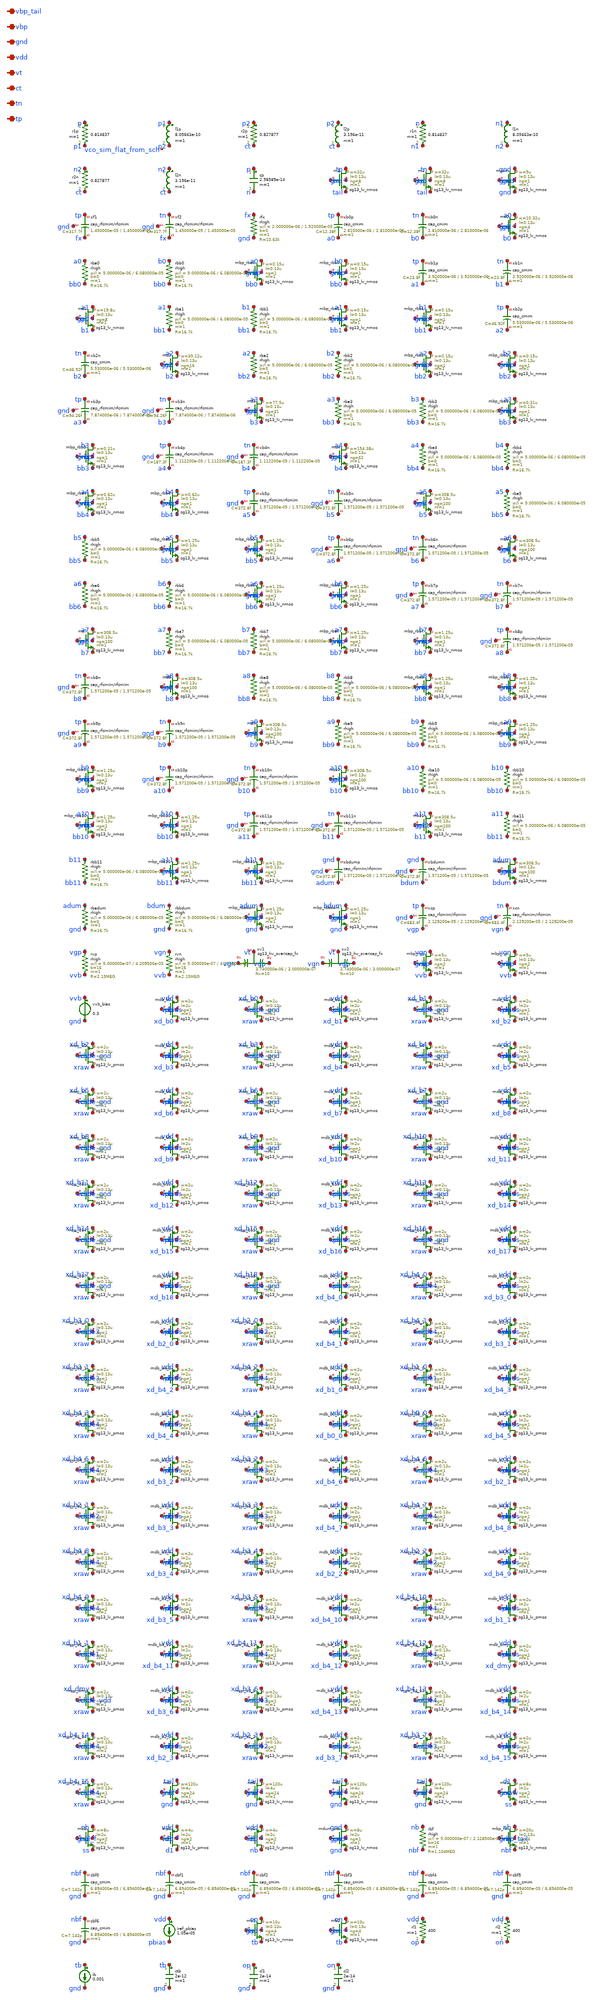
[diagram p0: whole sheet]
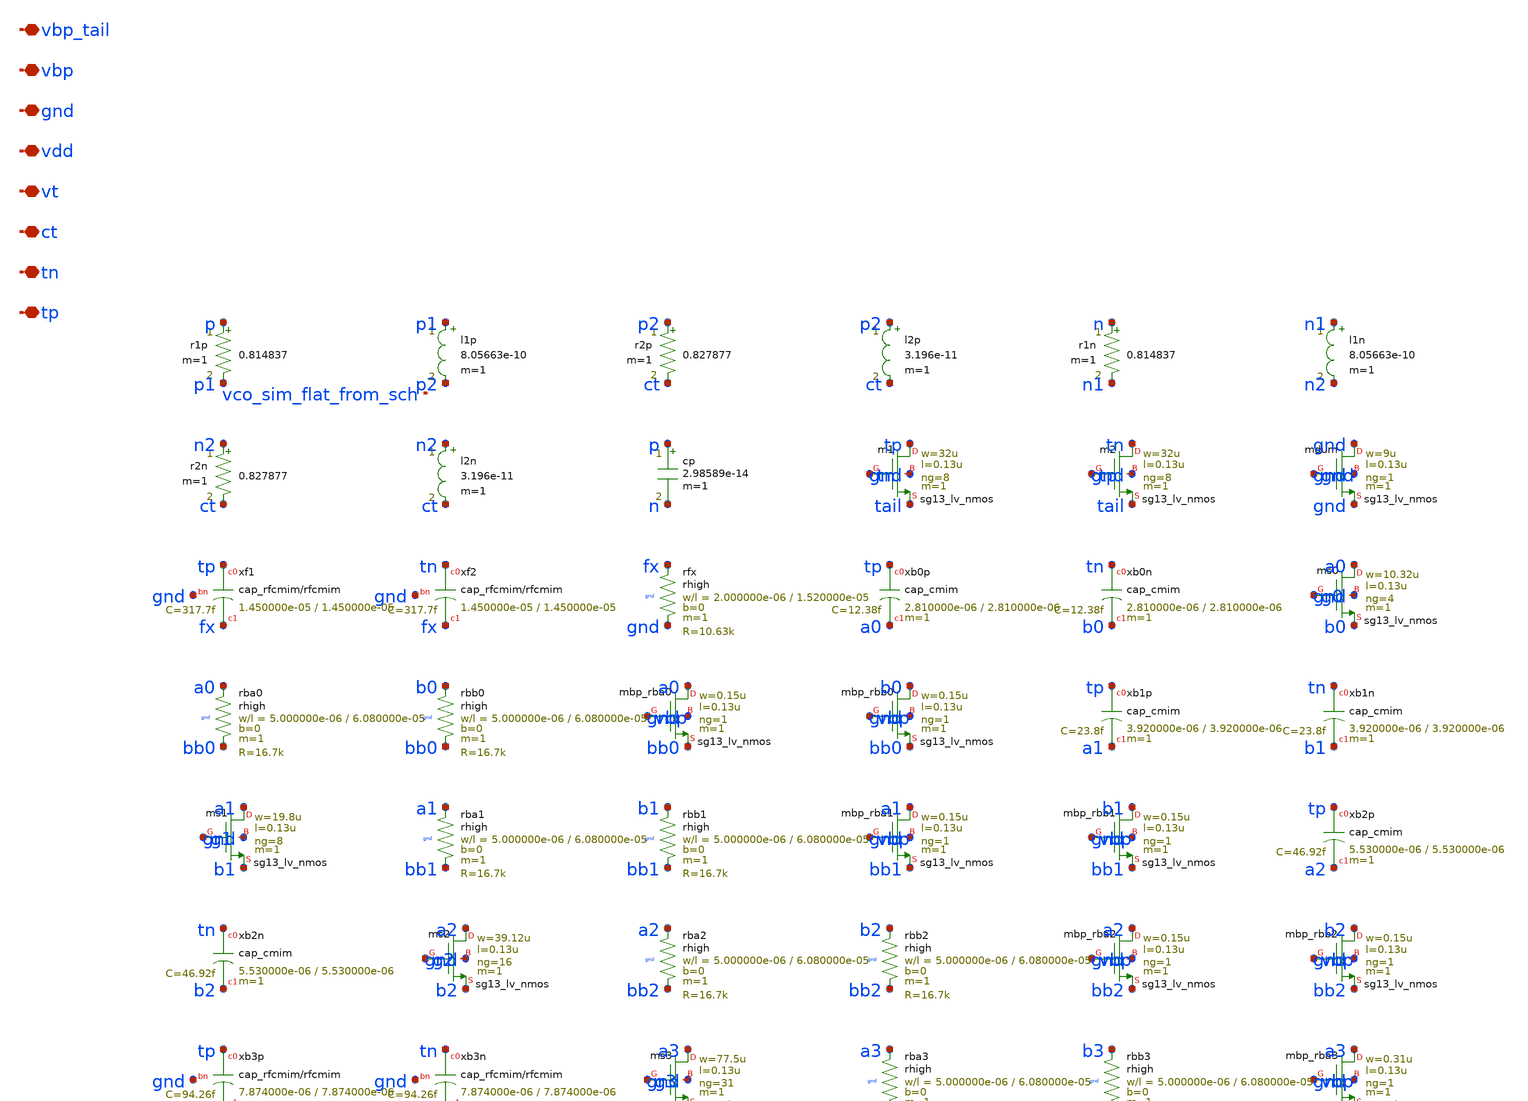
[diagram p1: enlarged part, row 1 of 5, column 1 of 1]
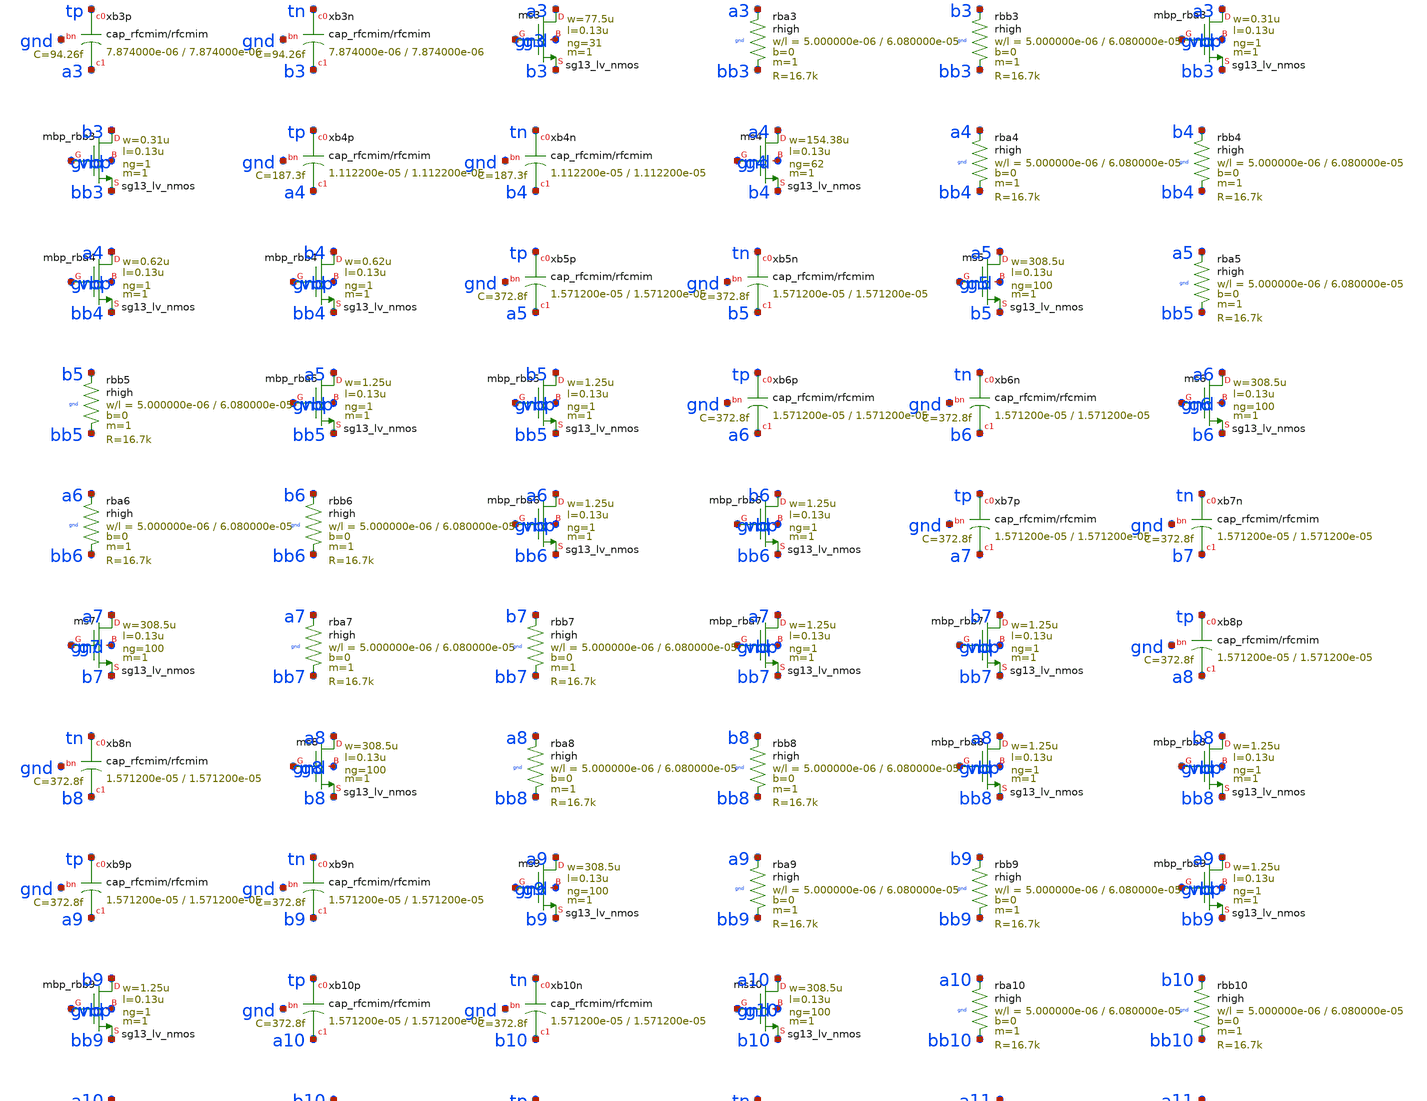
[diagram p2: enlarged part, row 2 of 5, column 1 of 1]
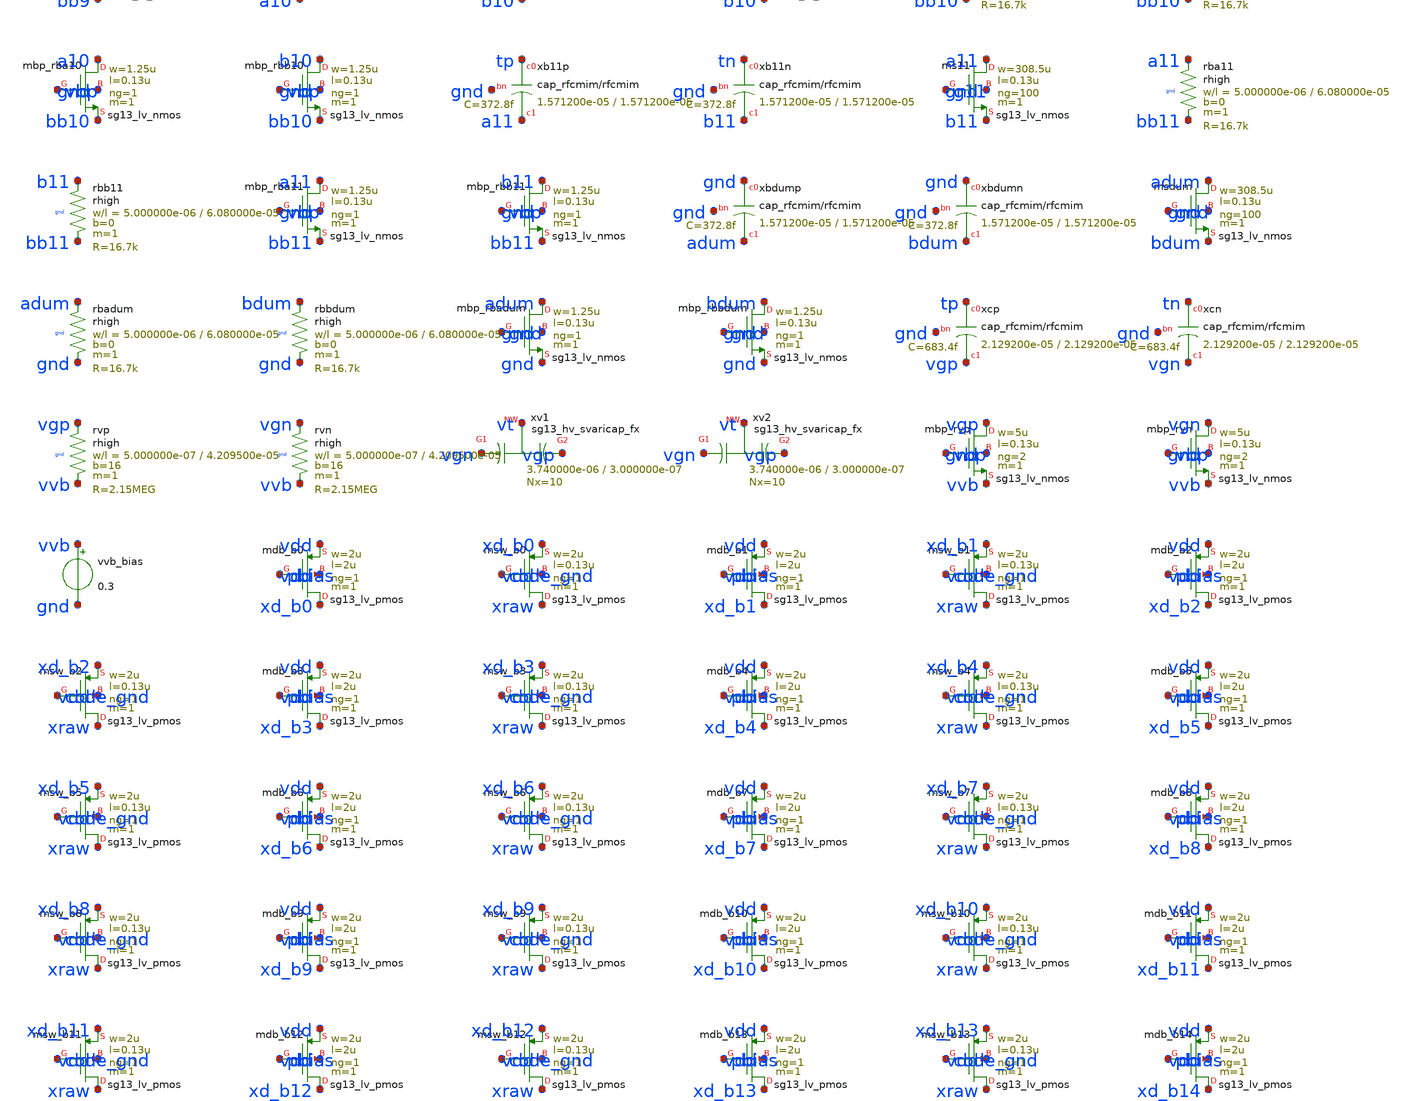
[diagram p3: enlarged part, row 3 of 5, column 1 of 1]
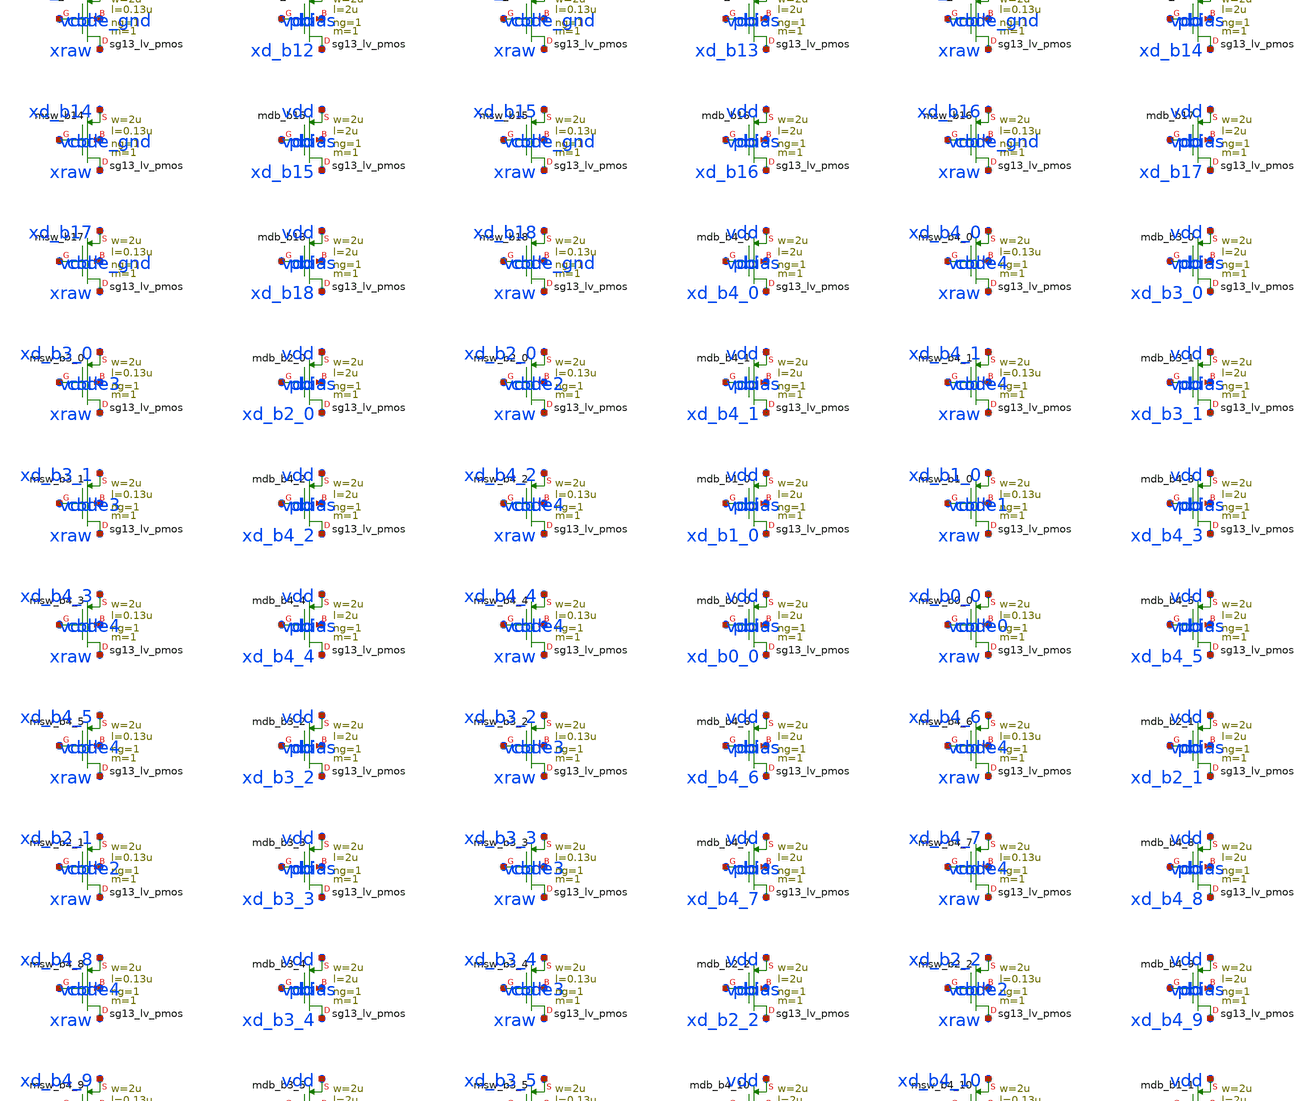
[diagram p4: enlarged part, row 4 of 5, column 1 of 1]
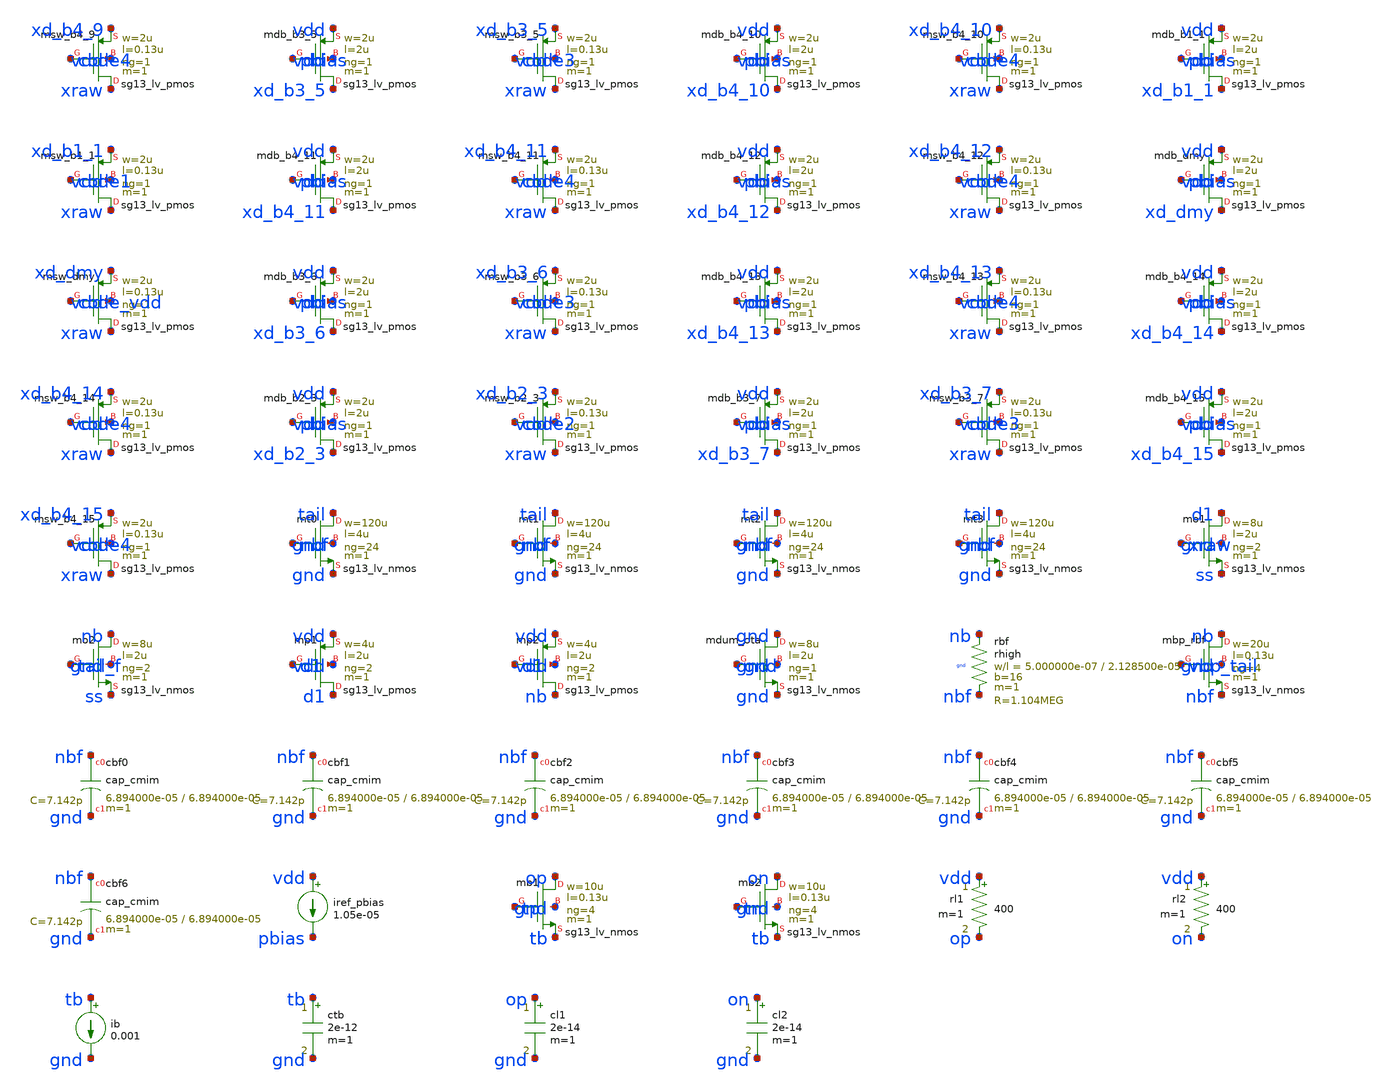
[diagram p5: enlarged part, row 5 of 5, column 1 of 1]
** sch_path: analog/vco/sch/vco_sim_flat.sch
**.subckt vco_sim_flat tp tn ct vt vdd gnd vbp vbp_tail
*.iopin tp
*.iopin tn
*.iopin ct
*.iopin vt
*.iopin vdd
*.iopin gnd
*.iopin vbp
*.iopin vbp_tail
r1p p p1 0.814837 m=1
l1p p1 p2 8.05663e-10 m=1
r2p p2 ct 0.827877 m=1
l2p p2 ct 3.196e-11 m=1
r1n n n1 0.814837 m=1
l1n n1 n2 8.05663e-10 m=1
r2n n2 ct 0.827877 m=1
l2n n2 ct 3.196e-11 m=1
cp p n 2.98589e-14 m=1
Xm1 tp tn tail gnd sg13_lv_nmos w=32u l=0.13u ng=8 m=1 mm_ok=1
Xm2 tn tp tail gnd sg13_lv_nmos w=32u l=0.13u ng=8 m=1 mm_ok=1
Xmdum gnd gnd gnd gnd sg13_lv_nmos w=9u l=0.13u ng=1 m=1 mm_ok=1
Xxf1 tp fx gnd cap_rfcmim w=1.450000e-05 l=1.450000e-05 wfeed=5.0e-6 m=1 mm_ok=1
Xxf2 tn fx gnd cap_rfcmim w=1.450000e-05 l=1.450000e-05 wfeed=5.0e-6 m=1 mm_ok=1
Xrfx fx gnd gnd rhigh w=2.000000e-06 l=1.520000e-05 m=1 b=0 mm_ok=1
Xxb0p tp a0 cap_cmim w=2.810000e-06 l=2.810000e-06 m=1 mm_ok=1
Xxb0n tn b0 cap_cmim w=2.810000e-06 l=2.810000e-06 m=1 mm_ok=1
Xms0 a0 g0 b0 gnd sg13_lv_nmos w=10.32u l=0.13u ng=4 m=1 mm_ok=1
Xrba0 a0 bb0 gnd rhigh w=5.000000e-06 l=6.080000e-05 m=1 b=0 mm_ok=1
Xrbb0 b0 bb0 gnd rhigh w=5.000000e-06 l=6.080000e-05 m=1 b=0 mm_ok=1
Xmbp_rba0 a0 vbp bb0 gnd sg13_lv_nmos w=0.15u l=0.13u ng=1 m=1 mm_ok=1
Xmbp_rbb0 b0 vbp bb0 gnd sg13_lv_nmos w=0.15u l=0.13u ng=1 m=1 mm_ok=1
Xxb1p tp a1 cap_cmim w=3.920000e-06 l=3.920000e-06 m=1 mm_ok=1
Xxb1n tn b1 cap_cmim w=3.920000e-06 l=3.920000e-06 m=1 mm_ok=1
Xms1 a1 g1 b1 gnd sg13_lv_nmos w=19.8u l=0.13u ng=8 m=1 mm_ok=1
Xrba1 a1 bb1 gnd rhigh w=5.000000e-06 l=6.080000e-05 m=1 b=0 mm_ok=1
Xrbb1 b1 bb1 gnd rhigh w=5.000000e-06 l=6.080000e-05 m=1 b=0 mm_ok=1
Xmbp_rba1 a1 vbp bb1 gnd sg13_lv_nmos w=0.15u l=0.13u ng=1 m=1 mm_ok=1
Xmbp_rbb1 b1 vbp bb1 gnd sg13_lv_nmos w=0.15u l=0.13u ng=1 m=1 mm_ok=1
Xxb2p tp a2 cap_cmim w=5.530000e-06 l=5.530000e-06 m=1 mm_ok=1
Xxb2n tn b2 cap_cmim w=5.530000e-06 l=5.530000e-06 m=1 mm_ok=1
Xms2 a2 g2 b2 gnd sg13_lv_nmos w=39.12u l=0.13u ng=16 m=1 mm_ok=1
Xrba2 a2 bb2 gnd rhigh w=5.000000e-06 l=6.080000e-05 m=1 b=0 mm_ok=1
Xrbb2 b2 bb2 gnd rhigh w=5.000000e-06 l=6.080000e-05 m=1 b=0 mm_ok=1
Xmbp_rba2 a2 vbp bb2 gnd sg13_lv_nmos w=0.15u l=0.13u ng=1 m=1 mm_ok=1
Xmbp_rbb2 b2 vbp bb2 gnd sg13_lv_nmos w=0.15u l=0.13u ng=1 m=1 mm_ok=1
Xxb3p tp a3 gnd cap_rfcmim w=7.874000e-06 l=7.874000e-06 wfeed=5.0e-6 m=1 mm_ok=1
Xxb3n tn b3 gnd cap_rfcmim w=7.874000e-06 l=7.874000e-06 wfeed=5.0e-6 m=1 mm_ok=1
Xms3 a3 g3 b3 gnd sg13_lv_nmos w=77.5u l=0.13u ng=31 m=1 mm_ok=1
Xrba3 a3 bb3 gnd rhigh w=5.000000e-06 l=6.080000e-05 m=1 b=0 mm_ok=1
Xrbb3 b3 bb3 gnd rhigh w=5.000000e-06 l=6.080000e-05 m=1 b=0 mm_ok=1
Xmbp_rba3 a3 vbp bb3 gnd sg13_lv_nmos w=0.31u l=0.13u ng=1 m=1 mm_ok=1
Xmbp_rbb3 b3 vbp bb3 gnd sg13_lv_nmos w=0.31u l=0.13u ng=1 m=1 mm_ok=1
Xxb4p tp a4 gnd cap_rfcmim w=1.112200e-05 l=1.112200e-05 wfeed=5.0e-6 m=1 mm_ok=1
Xxb4n tn b4 gnd cap_rfcmim w=1.112200e-05 l=1.112200e-05 wfeed=5.0e-6 m=1 mm_ok=1
Xms4 a4 g4 b4 gnd sg13_lv_nmos w=154.38u l=0.13u ng=62 m=1 mm_ok=1
Xrba4 a4 bb4 gnd rhigh w=5.000000e-06 l=6.080000e-05 m=1 b=0 mm_ok=1
Xrbb4 b4 bb4 gnd rhigh w=5.000000e-06 l=6.080000e-05 m=1 b=0 mm_ok=1
Xmbp_rba4 a4 vbp bb4 gnd sg13_lv_nmos w=0.62u l=0.13u ng=1 m=1 mm_ok=1
Xmbp_rbb4 b4 vbp bb4 gnd sg13_lv_nmos w=0.62u l=0.13u ng=1 m=1 mm_ok=1
Xxb5p tp a5 gnd cap_rfcmim w=1.571200e-05 l=1.571200e-05 wfeed=5.0e-6 m=1 mm_ok=1
Xxb5n tn b5 gnd cap_rfcmim w=1.571200e-05 l=1.571200e-05 wfeed=5.0e-6 m=1 mm_ok=1
Xms5 a5 g5 b5 gnd sg13_lv_nmos w=308.5u l=0.13u ng=100 m=1 mm_ok=1
Xrba5 a5 bb5 gnd rhigh w=5.000000e-06 l=6.080000e-05 m=1 b=0 mm_ok=1
Xrbb5 b5 bb5 gnd rhigh w=5.000000e-06 l=6.080000e-05 m=1 b=0 mm_ok=1
Xmbp_rba5 a5 vbp bb5 gnd sg13_lv_nmos w=1.25u l=0.13u ng=1 m=1 mm_ok=1
Xmbp_rbb5 b5 vbp bb5 gnd sg13_lv_nmos w=1.25u l=0.13u ng=1 m=1 mm_ok=1
Xxb6p tp a6 gnd cap_rfcmim w=1.571200e-05 l=1.571200e-05 wfeed=5.0e-6 m=1 mm_ok=1
Xxb6n tn b6 gnd cap_rfcmim w=1.571200e-05 l=1.571200e-05 wfeed=5.0e-6 m=1 mm_ok=1
Xms6 a6 g6 b6 gnd sg13_lv_nmos w=308.5u l=0.13u ng=100 m=1 mm_ok=1
Xrba6 a6 bb6 gnd rhigh w=5.000000e-06 l=6.080000e-05 m=1 b=0 mm_ok=1
Xrbb6 b6 bb6 gnd rhigh w=5.000000e-06 l=6.080000e-05 m=1 b=0 mm_ok=1
Xmbp_rba6 a6 vbp bb6 gnd sg13_lv_nmos w=1.25u l=0.13u ng=1 m=1 mm_ok=1
Xmbp_rbb6 b6 vbp bb6 gnd sg13_lv_nmos w=1.25u l=0.13u ng=1 m=1 mm_ok=1
Xxb7p tp a7 gnd cap_rfcmim w=1.571200e-05 l=1.571200e-05 wfeed=5.0e-6 m=1 mm_ok=1
Xxb7n tn b7 gnd cap_rfcmim w=1.571200e-05 l=1.571200e-05 wfeed=5.0e-6 m=1 mm_ok=1
Xms7 a7 g7 b7 gnd sg13_lv_nmos w=308.5u l=0.13u ng=100 m=1 mm_ok=1
Xrba7 a7 bb7 gnd rhigh w=5.000000e-06 l=6.080000e-05 m=1 b=0 mm_ok=1
Xrbb7 b7 bb7 gnd rhigh w=5.000000e-06 l=6.080000e-05 m=1 b=0 mm_ok=1
Xmbp_rba7 a7 vbp bb7 gnd sg13_lv_nmos w=1.25u l=0.13u ng=1 m=1 mm_ok=1
Xmbp_rbb7 b7 vbp bb7 gnd sg13_lv_nmos w=1.25u l=0.13u ng=1 m=1 mm_ok=1
Xxb8p tp a8 gnd cap_rfcmim w=1.571200e-05 l=1.571200e-05 wfeed=5.0e-6 m=1 mm_ok=1
Xxb8n tn b8 gnd cap_rfcmim w=1.571200e-05 l=1.571200e-05 wfeed=5.0e-6 m=1 mm_ok=1
Xms8 a8 g8 b8 gnd sg13_lv_nmos w=308.5u l=0.13u ng=100 m=1 mm_ok=1
Xrba8 a8 bb8 gnd rhigh w=5.000000e-06 l=6.080000e-05 m=1 b=0 mm_ok=1
Xrbb8 b8 bb8 gnd rhigh w=5.000000e-06 l=6.080000e-05 m=1 b=0 mm_ok=1
Xmbp_rba8 a8 vbp bb8 gnd sg13_lv_nmos w=1.25u l=0.13u ng=1 m=1 mm_ok=1
Xmbp_rbb8 b8 vbp bb8 gnd sg13_lv_nmos w=1.25u l=0.13u ng=1 m=1 mm_ok=1
Xxb9p tp a9 gnd cap_rfcmim w=1.571200e-05 l=1.571200e-05 wfeed=5.0e-6 m=1 mm_ok=1
Xxb9n tn b9 gnd cap_rfcmim w=1.571200e-05 l=1.571200e-05 wfeed=5.0e-6 m=1 mm_ok=1
Xms9 a9 g9 b9 gnd sg13_lv_nmos w=308.5u l=0.13u ng=100 m=1 mm_ok=1
Xrba9 a9 bb9 gnd rhigh w=5.000000e-06 l=6.080000e-05 m=1 b=0 mm_ok=1
Xrbb9 b9 bb9 gnd rhigh w=5.000000e-06 l=6.080000e-05 m=1 b=0 mm_ok=1
Xmbp_rba9 a9 vbp bb9 gnd sg13_lv_nmos w=1.25u l=0.13u ng=1 m=1 mm_ok=1
Xmbp_rbb9 b9 vbp bb9 gnd sg13_lv_nmos w=1.25u l=0.13u ng=1 m=1 mm_ok=1
Xxb10p tp a10 gnd cap_rfcmim w=1.571200e-05 l=1.571200e-05 wfeed=5.0e-6 m=1 mm_ok=1
Xxb10n tn b10 gnd cap_rfcmim w=1.571200e-05 l=1.571200e-05 wfeed=5.0e-6 m=1 mm_ok=1
Xms10 a10 g10 b10 gnd sg13_lv_nmos w=308.5u l=0.13u ng=100 m=1 mm_ok=1
Xrba10 a10 bb10 gnd rhigh w=5.000000e-06 l=6.080000e-05 m=1 b=0 mm_ok=1
Xrbb10 b10 bb10 gnd rhigh w=5.000000e-06 l=6.080000e-05 m=1 b=0 mm_ok=1
Xmbp_rba10 a10 vbp bb10 gnd sg13_lv_nmos w=1.25u l=0.13u ng=1 m=1 mm_ok=1
Xmbp_rbb10 b10 vbp bb10 gnd sg13_lv_nmos w=1.25u l=0.13u ng=1 m=1 mm_ok=1
Xxb11p tp a11 gnd cap_rfcmim w=1.571200e-05 l=1.571200e-05 wfeed=5.0e-6 m=1 mm_ok=1
Xxb11n tn b11 gnd cap_rfcmim w=1.571200e-05 l=1.571200e-05 wfeed=5.0e-6 m=1 mm_ok=1
Xms11 a11 g11 b11 gnd sg13_lv_nmos w=308.5u l=0.13u ng=100 m=1 mm_ok=1
Xrba11 a11 bb11 gnd rhigh w=5.000000e-06 l=6.080000e-05 m=1 b=0 mm_ok=1
Xrbb11 b11 bb11 gnd rhigh w=5.000000e-06 l=6.080000e-05 m=1 b=0 mm_ok=1
Xmbp_rba11 a11 vbp bb11 gnd sg13_lv_nmos w=1.25u l=0.13u ng=1 m=1 mm_ok=1
Xmbp_rbb11 b11 vbp bb11 gnd sg13_lv_nmos w=1.25u l=0.13u ng=1 m=1 mm_ok=1
Xxbdump gnd adum gnd cap_rfcmim w=1.571200e-05 l=1.571200e-05 wfeed=5.0e-6 m=1 mm_ok=1
Xxbdumn gnd bdum gnd cap_rfcmim w=1.571200e-05 l=1.571200e-05 wfeed=5.0e-6 m=1 mm_ok=1
Xmsdum adum gnd bdum gnd sg13_lv_nmos w=308.5u l=0.13u ng=100 m=1 mm_ok=1
Xrbadum adum gnd gnd rhigh w=5.000000e-06 l=6.080000e-05 m=1 b=0 mm_ok=1
Xrbbdum bdum gnd gnd rhigh w=5.000000e-06 l=6.080000e-05 m=1 b=0 mm_ok=1
Xmbp_rbadum adum gnd gnd gnd sg13_lv_nmos w=1.25u l=0.13u ng=1 m=1 mm_ok=1
Xmbp_rbbdum bdum gnd gnd gnd sg13_lv_nmos w=1.25u l=0.13u ng=1 m=1 mm_ok=1
Xxcp tp vgp gnd cap_rfcmim w=2.129200e-05 l=2.129200e-05 wfeed=5.0e-6 m=1 mm_ok=1
Xxcn tn vgn gnd cap_rfcmim w=2.129200e-05 l=2.129200e-05 wfeed=5.0e-6 m=1 mm_ok=1
Xrvp vgp vvb gnd rhigh w=5.000000e-07 l=4.209500e-05 m=1 b=16 mm_ok=1
Xrvn vgn vvb gnd rhigh w=5.000000e-07 l=4.209500e-05 m=1 b=16 mm_ok=1
Xxv1 vgn vt vgp sub! sg13_hv_svaricap_fx w=3.740000e-06 l=3.000000e-07 Nx=10 mm_ok=1
Xxv2 vgn vt vgp sub! sg13_hv_svaricap_fx w=3.740000e-06 l=3.000000e-07 Nx=10 mm_ok=1
Xmbp_rvp vgp vbp vvb gnd sg13_lv_nmos w=5u l=0.13u ng=2 m=1 mm_ok=1
Xmbp_rvn vgn vbp vvb gnd sg13_lv_nmos w=5u l=0.13u ng=2 m=1 mm_ok=1
vvb_bias vvb gnd 0.3
Xmdb_b0 xd_b0 pbias vdd vdd sg13_lv_pmos w=2u l=2u ng=1 m=1 mm_ok=1
Xmsw_b0 xraw code_gnd xd_b0 vdd sg13_lv_pmos w=2u l=0.13u ng=1 m=1 mm_ok=1
Xmdb_b1 xd_b1 pbias vdd vdd sg13_lv_pmos w=2u l=2u ng=1 m=1 mm_ok=1
Xmsw_b1 xraw code_gnd xd_b1 vdd sg13_lv_pmos w=2u l=0.13u ng=1 m=1 mm_ok=1
Xmdb_b2 xd_b2 pbias vdd vdd sg13_lv_pmos w=2u l=2u ng=1 m=1 mm_ok=1
Xmsw_b2 xraw code_gnd xd_b2 vdd sg13_lv_pmos w=2u l=0.13u ng=1 m=1 mm_ok=1
Xmdb_b3 xd_b3 pbias vdd vdd sg13_lv_pmos w=2u l=2u ng=1 m=1 mm_ok=1
Xmsw_b3 xraw code_gnd xd_b3 vdd sg13_lv_pmos w=2u l=0.13u ng=1 m=1 mm_ok=1
Xmdb_b4 xd_b4 pbias vdd vdd sg13_lv_pmos w=2u l=2u ng=1 m=1 mm_ok=1
Xmsw_b4 xraw code_gnd xd_b4 vdd sg13_lv_pmos w=2u l=0.13u ng=1 m=1 mm_ok=1
Xmdb_b5 xd_b5 pbias vdd vdd sg13_lv_pmos w=2u l=2u ng=1 m=1 mm_ok=1
Xmsw_b5 xraw code_gnd xd_b5 vdd sg13_lv_pmos w=2u l=0.13u ng=1 m=1 mm_ok=1
Xmdb_b6 xd_b6 pbias vdd vdd sg13_lv_pmos w=2u l=2u ng=1 m=1 mm_ok=1
Xmsw_b6 xraw code_gnd xd_b6 vdd sg13_lv_pmos w=2u l=0.13u ng=1 m=1 mm_ok=1
Xmdb_b7 xd_b7 pbias vdd vdd sg13_lv_pmos w=2u l=2u ng=1 m=1 mm_ok=1
Xmsw_b7 xraw code_gnd xd_b7 vdd sg13_lv_pmos w=2u l=0.13u ng=1 m=1 mm_ok=1
Xmdb_b8 xd_b8 pbias vdd vdd sg13_lv_pmos w=2u l=2u ng=1 m=1 mm_ok=1
Xmsw_b8 xraw code_gnd xd_b8 vdd sg13_lv_pmos w=2u l=0.13u ng=1 m=1 mm_ok=1
Xmdb_b9 xd_b9 pbias vdd vdd sg13_lv_pmos w=2u l=2u ng=1 m=1 mm_ok=1
Xmsw_b9 xraw code_gnd xd_b9 vdd sg13_lv_pmos w=2u l=0.13u ng=1 m=1 mm_ok=1
Xmdb_b10 xd_b10 pbias vdd vdd sg13_lv_pmos w=2u l=2u ng=1 m=1 mm_ok=1
Xmsw_b10 xraw code_gnd xd_b10 vdd sg13_lv_pmos w=2u l=0.13u ng=1 m=1 mm_ok=1
Xmdb_b11 xd_b11 pbias vdd vdd sg13_lv_pmos w=2u l=2u ng=1 m=1 mm_ok=1
Xmsw_b11 xraw code_gnd xd_b11 vdd sg13_lv_pmos w=2u l=0.13u ng=1 m=1 mm_ok=1
Xmdb_b12 xd_b12 pbias vdd vdd sg13_lv_pmos w=2u l=2u ng=1 m=1 mm_ok=1
Xmsw_b12 xraw code_gnd xd_b12 vdd sg13_lv_pmos w=2u l=0.13u ng=1 m=1 mm_ok=1
Xmdb_b13 xd_b13 pbias vdd vdd sg13_lv_pmos w=2u l=2u ng=1 m=1 mm_ok=1
Xmsw_b13 xraw code_gnd xd_b13 vdd sg13_lv_pmos w=2u l=0.13u ng=1 m=1 mm_ok=1
Xmdb_b14 xd_b14 pbias vdd vdd sg13_lv_pmos w=2u l=2u ng=1 m=1 mm_ok=1
Xmsw_b14 xraw code_gnd xd_b14 vdd sg13_lv_pmos w=2u l=0.13u ng=1 m=1 mm_ok=1
Xmdb_b15 xd_b15 pbias vdd vdd sg13_lv_pmos w=2u l=2u ng=1 m=1 mm_ok=1
Xmsw_b15 xraw code_gnd xd_b15 vdd sg13_lv_pmos w=2u l=0.13u ng=1 m=1 mm_ok=1
Xmdb_b16 xd_b16 pbias vdd vdd sg13_lv_pmos w=2u l=2u ng=1 m=1 mm_ok=1
Xmsw_b16 xraw code_gnd xd_b16 vdd sg13_lv_pmos w=2u l=0.13u ng=1 m=1 mm_ok=1
Xmdb_b17 xd_b17 pbias vdd vdd sg13_lv_pmos w=2u l=2u ng=1 m=1 mm_ok=1
Xmsw_b17 xraw code_gnd xd_b17 vdd sg13_lv_pmos w=2u l=0.13u ng=1 m=1 mm_ok=1
Xmdb_b18 xd_b18 pbias vdd vdd sg13_lv_pmos w=2u l=2u ng=1 m=1 mm_ok=1
Xmsw_b18 xraw code_gnd xd_b18 vdd sg13_lv_pmos w=2u l=0.13u ng=1 m=1 mm_ok=1
Xmdb_b4_0 xd_b4_0 pbias vdd vdd sg13_lv_pmos w=2u l=2u ng=1 m=1 mm_ok=1
Xmsw_b4_0 xraw code4 xd_b4_0 vdd sg13_lv_pmos w=2u l=0.13u ng=1 m=1 mm_ok=1
Xmdb_b3_0 xd_b3_0 pbias vdd vdd sg13_lv_pmos w=2u l=2u ng=1 m=1 mm_ok=1
Xmsw_b3_0 xraw code3 xd_b3_0 vdd sg13_lv_pmos w=2u l=0.13u ng=1 m=1 mm_ok=1
Xmdb_b2_0 xd_b2_0 pbias vdd vdd sg13_lv_pmos w=2u l=2u ng=1 m=1 mm_ok=1
Xmsw_b2_0 xraw code2 xd_b2_0 vdd sg13_lv_pmos w=2u l=0.13u ng=1 m=1 mm_ok=1
Xmdb_b4_1 xd_b4_1 pbias vdd vdd sg13_lv_pmos w=2u l=2u ng=1 m=1 mm_ok=1
Xmsw_b4_1 xraw code4 xd_b4_1 vdd sg13_lv_pmos w=2u l=0.13u ng=1 m=1 mm_ok=1
Xmdb_b3_1 xd_b3_1 pbias vdd vdd sg13_lv_pmos w=2u l=2u ng=1 m=1 mm_ok=1
Xmsw_b3_1 xraw code3 xd_b3_1 vdd sg13_lv_pmos w=2u l=0.13u ng=1 m=1 mm_ok=1
Xmdb_b4_2 xd_b4_2 pbias vdd vdd sg13_lv_pmos w=2u l=2u ng=1 m=1 mm_ok=1
Xmsw_b4_2 xraw code4 xd_b4_2 vdd sg13_lv_pmos w=2u l=0.13u ng=1 m=1 mm_ok=1
Xmdb_b1_0 xd_b1_0 pbias vdd vdd sg13_lv_pmos w=2u l=2u ng=1 m=1 mm_ok=1
Xmsw_b1_0 xraw code1 xd_b1_0 vdd sg13_lv_pmos w=2u l=0.13u ng=1 m=1 mm_ok=1
Xmdb_b4_3 xd_b4_3 pbias vdd vdd sg13_lv_pmos w=2u l=2u ng=1 m=1 mm_ok=1
Xmsw_b4_3 xraw code4 xd_b4_3 vdd sg13_lv_pmos w=2u l=0.13u ng=1 m=1 mm_ok=1
Xmdb_b4_4 xd_b4_4 pbias vdd vdd sg13_lv_pmos w=2u l=2u ng=1 m=1 mm_ok=1
Xmsw_b4_4 xraw code4 xd_b4_4 vdd sg13_lv_pmos w=2u l=0.13u ng=1 m=1 mm_ok=1
Xmdb_b0_0 xd_b0_0 pbias vdd vdd sg13_lv_pmos w=2u l=2u ng=1 m=1 mm_ok=1
Xmsw_b0_0 xraw code0 xd_b0_0 vdd sg13_lv_pmos w=2u l=0.13u ng=1 m=1 mm_ok=1
Xmdb_b4_5 xd_b4_5 pbias vdd vdd sg13_lv_pmos w=2u l=2u ng=1 m=1 mm_ok=1
Xmsw_b4_5 xraw code4 xd_b4_5 vdd sg13_lv_pmos w=2u l=0.13u ng=1 m=1 mm_ok=1
Xmdb_b3_2 xd_b3_2 pbias vdd vdd sg13_lv_pmos w=2u l=2u ng=1 m=1 mm_ok=1
Xmsw_b3_2 xraw code3 xd_b3_2 vdd sg13_lv_pmos w=2u l=0.13u ng=1 m=1 mm_ok=1
Xmdb_b4_6 xd_b4_6 pbias vdd vdd sg13_lv_pmos w=2u l=2u ng=1 m=1 mm_ok=1
Xmsw_b4_6 xraw code4 xd_b4_6 vdd sg13_lv_pmos w=2u l=0.13u ng=1 m=1 mm_ok=1
Xmdb_b2_1 xd_b2_1 pbias vdd vdd sg13_lv_pmos w=2u l=2u ng=1 m=1 mm_ok=1
Xmsw_b2_1 xraw code2 xd_b2_1 vdd sg13_lv_pmos w=2u l=0.13u ng=1 m=1 mm_ok=1
Xmdb_b3_3 xd_b3_3 pbias vdd vdd sg13_lv_pmos w=2u l=2u ng=1 m=1 mm_ok=1
Xmsw_b3_3 xraw code3 xd_b3_3 vdd sg13_lv_pmos w=2u l=0.13u ng=1 m=1 mm_ok=1
Xmdb_b4_7 xd_b4_7 pbias vdd vdd sg13_lv_pmos w=2u l=2u ng=1 m=1 mm_ok=1
Xmsw_b4_7 xraw code4 xd_b4_7 vdd sg13_lv_pmos w=2u l=0.13u ng=1 m=1 mm_ok=1
Xmdb_b4_8 xd_b4_8 pbias vdd vdd sg13_lv_pmos w=2u l=2u ng=1 m=1 mm_ok=1
Xmsw_b4_8 xraw code4 xd_b4_8 vdd sg13_lv_pmos w=2u l=0.13u ng=1 m=1 mm_ok=1
Xmdb_b3_4 xd_b3_4 pbias vdd vdd sg13_lv_pmos w=2u l=2u ng=1 m=1 mm_ok=1
Xmsw_b3_4 xraw code3 xd_b3_4 vdd sg13_lv_pmos w=2u l=0.13u ng=1 m=1 mm_ok=1
Xmdb_b2_2 xd_b2_2 pbias vdd vdd sg13_lv_pmos w=2u l=2u ng=1 m=1 mm_ok=1
Xmsw_b2_2 xraw code2 xd_b2_2 vdd sg13_lv_pmos w=2u l=0.13u ng=1 m=1 mm_ok=1
Xmdb_b4_9 xd_b4_9 pbias vdd vdd sg13_lv_pmos w=2u l=2u ng=1 m=1 mm_ok=1
Xmsw_b4_9 xraw code4 xd_b4_9 vdd sg13_lv_pmos w=2u l=0.13u ng=1 m=1 mm_ok=1
Xmdb_b3_5 xd_b3_5 pbias vdd vdd sg13_lv_pmos w=2u l=2u ng=1 m=1 mm_ok=1
Xmsw_b3_5 xraw code3 xd_b3_5 vdd sg13_lv_pmos w=2u l=0.13u ng=1 m=1 mm_ok=1
Xmdb_b4_10 xd_b4_10 pbias vdd vdd sg13_lv_pmos w=2u l=2u ng=1 m=1 mm_ok=1
Xmsw_b4_10 xraw code4 xd_b4_10 vdd sg13_lv_pmos w=2u l=0.13u ng=1 m=1 mm_ok=1
Xmdb_b1_1 xd_b1_1 pbias vdd vdd sg13_lv_pmos w=2u l=2u ng=1 m=1 mm_ok=1
Xmsw_b1_1 xraw code1 xd_b1_1 vdd sg13_lv_pmos w=2u l=0.13u ng=1 m=1 mm_ok=1
Xmdb_b4_11 xd_b4_11 pbias vdd vdd sg13_lv_pmos w=2u l=2u ng=1 m=1 mm_ok=1
Xmsw_b4_11 xraw code4 xd_b4_11 vdd sg13_lv_pmos w=2u l=0.13u ng=1 m=1 mm_ok=1
Xmdb_b4_12 xd_b4_12 pbias vdd vdd sg13_lv_pmos w=2u l=2u ng=1 m=1 mm_ok=1
Xmsw_b4_12 xraw code4 xd_b4_12 vdd sg13_lv_pmos w=2u l=0.13u ng=1 m=1 mm_ok=1
Xmdb_dmy xd_dmy pbias vdd vdd sg13_lv_pmos w=2u l=2u ng=1 m=1 mm_ok=1
Xmsw_dmy xraw code_vdd xd_dmy vdd sg13_lv_pmos w=2u l=0.13u ng=1 m=1 mm_ok=1
Xmdb_b3_6 xd_b3_6 pbias vdd vdd sg13_lv_pmos w=2u l=2u ng=1 m=1 mm_ok=1
Xmsw_b3_6 xraw code3 xd_b3_6 vdd sg13_lv_pmos w=2u l=0.13u ng=1 m=1 mm_ok=1
Xmdb_b4_13 xd_b4_13 pbias vdd vdd sg13_lv_pmos w=2u l=2u ng=1 m=1 mm_ok=1
Xmsw_b4_13 xraw code4 xd_b4_13 vdd sg13_lv_pmos w=2u l=0.13u ng=1 m=1 mm_ok=1
Xmdb_b4_14 xd_b4_14 pbias vdd vdd sg13_lv_pmos w=2u l=2u ng=1 m=1 mm_ok=1
Xmsw_b4_14 xraw code4 xd_b4_14 vdd sg13_lv_pmos w=2u l=0.13u ng=1 m=1 mm_ok=1
Xmdb_b2_3 xd_b2_3 pbias vdd vdd sg13_lv_pmos w=2u l=2u ng=1 m=1 mm_ok=1
Xmsw_b2_3 xraw code2 xd_b2_3 vdd sg13_lv_pmos w=2u l=0.13u ng=1 m=1 mm_ok=1
Xmdb_b3_7 xd_b3_7 pbias vdd vdd sg13_lv_pmos w=2u l=2u ng=1 m=1 mm_ok=1
Xmsw_b3_7 xraw code3 xd_b3_7 vdd sg13_lv_pmos w=2u l=0.13u ng=1 m=1 mm_ok=1
Xmdb_b4_15 xd_b4_15 pbias vdd vdd sg13_lv_pmos w=2u l=2u ng=1 m=1 mm_ok=1
Xmsw_b4_15 xraw code4 xd_b4_15 vdd sg13_lv_pmos w=2u l=0.13u ng=1 m=1 mm_ok=1
Xmt0 tail nbf gnd gnd sg13_lv_nmos w=120u l=4u ng=24 m=1 mm_ok=1
Xmt1 tail nbf gnd gnd sg13_lv_nmos w=120u l=4u ng=24 m=1 mm_ok=1
Xmt2 tail nbf gnd gnd sg13_lv_nmos w=120u l=4u ng=24 m=1 mm_ok=1
Xmt3 tail nbf gnd gnd sg13_lv_nmos w=120u l=4u ng=24 m=1 mm_ok=1
Xmo1 d1 xraw ss gnd sg13_lv_nmos w=8u l=2u ng=2 m=1 mm_ok=1
Xmo2 nb tail_f ss gnd sg13_lv_nmos w=8u l=2u ng=2 m=1 mm_ok=1
Xmp1 d1 d1 vdd vdd sg13_lv_pmos w=4u l=2u ng=2 m=1 mm_ok=1
Xmp2 nb d1 vdd vdd sg13_lv_pmos w=4u l=2u ng=2 m=1 mm_ok=1
Xmdum_ota gnd gnd gnd gnd sg13_lv_nmos w=8u l=2u ng=1 m=1 mm_ok=1
Xrbf nb nbf gnd rhigh w=5.000000e-07 l=2.128500e-05 m=1 b=16 mm_ok=1
Xmbp_rbf nb vbp_tail nbf gnd sg13_lv_nmos w=20u l=0.13u ng=4 m=1 mm_ok=1
Xcbf0 nbf gnd cap_cmim w=6.894000e-05 l=6.894000e-05 m=1 mm_ok=1
Xcbf1 nbf gnd cap_cmim w=6.894000e-05 l=6.894000e-05 m=1 mm_ok=1
Xcbf2 nbf gnd cap_cmim w=6.894000e-05 l=6.894000e-05 m=1 mm_ok=1
Xcbf3 nbf gnd cap_cmim w=6.894000e-05 l=6.894000e-05 m=1 mm_ok=1
Xcbf4 nbf gnd cap_cmim w=6.894000e-05 l=6.894000e-05 m=1 mm_ok=1
Xcbf5 nbf gnd cap_cmim w=6.894000e-05 l=6.894000e-05 m=1 mm_ok=1
Xcbf6 nbf gnd cap_cmim w=6.894000e-05 l=6.894000e-05 m=1 mm_ok=1
iref_pbias vdd pbias 1.05e-05
Xmb1 op tp tb gnd sg13_lv_nmos w=10u l=0.13u ng=4 m=1 mm_ok=1
Xmb2 on tn tb gnd sg13_lv_nmos w=10u l=0.13u ng=4 m=1 mm_ok=1
rl1 vdd op 400 m=1
rl2 vdd on 400 m=1
ib tb gnd 0.001
ctb tb gnd 2e-12 m=1
cl1 op gnd 2e-14 m=1
cl2 on gnd 2e-14 m=1
**.ends
.end
